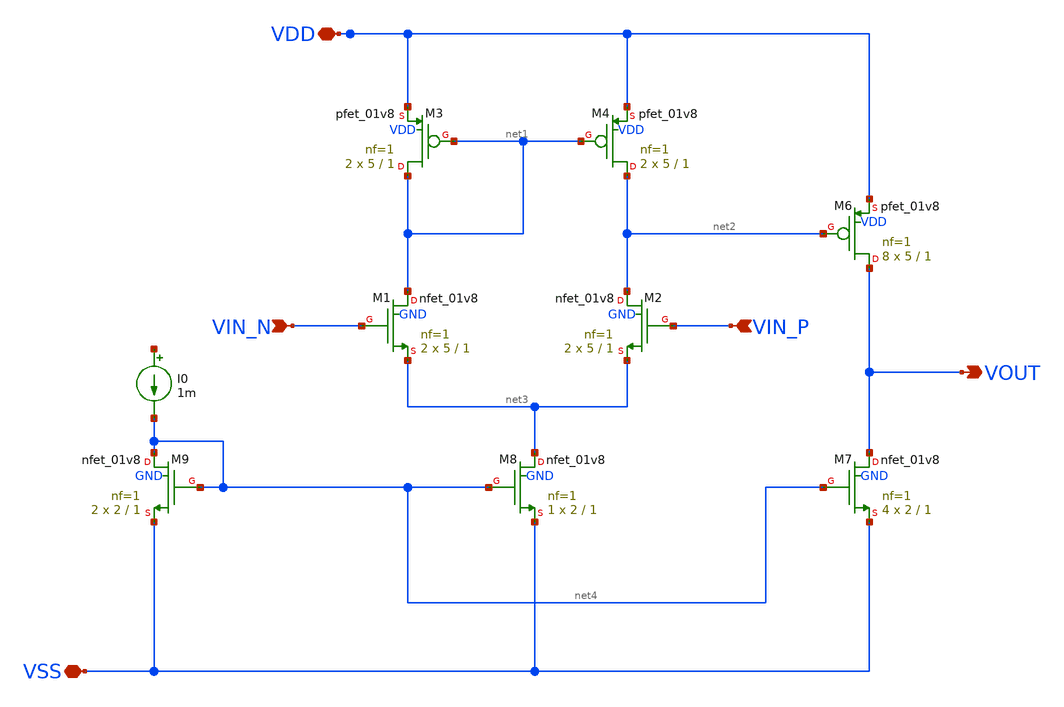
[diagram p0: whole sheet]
** sch_path: analog/schematics/opamp_two_stage.sch
**.subckt opamp_two_stage VDD VSS VOUT VIN_P VIN_N
*.iopin VDD
*.iopin VSS
*.opin VOUT
*.ipin VIN_P
*.ipin VIN_N
XM1 net1 VIN_N net3 GND sky130_fd_pr__nfet_01v8 L=1 W=5 nf=1 ad='int((nf+1)/2) * W/nf * 0.29' as='int((nf+2)/2) * W/nf * 0.29'
+ pd='2*int((nf+1)/2) * (W/nf + 0.29)' ps='2*int((nf+2)/2) * (W/nf + 0.29)' nrd='0.29 / W' nrs='0.29 / W'
+ sa=0 sb=0 sd=0 mult=2 m=2
XM2 net2 VIN_P net3 GND sky130_fd_pr__nfet_01v8 L=1 W=5 nf=1 ad='int((nf+1)/2) * W/nf * 0.29' as='int((nf+2)/2) * W/nf * 0.29'
+ pd='2*int((nf+1)/2) * (W/nf + 0.29)' ps='2*int((nf+2)/2) * (W/nf + 0.29)' nrd='0.29 / W' nrs='0.29 / W'
+ sa=0 sb=0 sd=0 mult=2 m=2
XM7 VOUT net4 VSS GND sky130_fd_pr__nfet_01v8 L=1 W=2 nf=1 ad='int((nf+1)/2) * W/nf * 0.29' as='int((nf+2)/2) * W/nf * 0.29'
+ pd='2*int((nf+1)/2) * (W/nf + 0.29)' ps='2*int((nf+2)/2) * (W/nf + 0.29)' nrd='0.29 / W' nrs='0.29 / W'
+ sa=0 sb=0 sd=0 mult=4 m=4
XM8 net3 net4 VSS GND sky130_fd_pr__nfet_01v8 L=1 W=2 nf=1 ad='int((nf+1)/2) * W/nf * 0.29' as='int((nf+2)/2) * W/nf * 0.29'
+ pd='2*int((nf+1)/2) * (W/nf + 0.29)' ps='2*int((nf+2)/2) * (W/nf + 0.29)' nrd='0.29 / W' nrs='0.29 / W'
+ sa=0 sb=0 sd=0 mult=1 m=1
XM3 net1 net1 VDD VDD sky130_fd_pr__pfet_01v8 L=1 W=5 nf=1 ad='int((nf+1)/2) * W/nf * 0.29' as='int((nf+2)/2) * W/nf * 0.29'
+ pd='2*int((nf+1)/2) * (W/nf + 0.29)' ps='2*int((nf+2)/2) * (W/nf + 0.29)' nrd='0.29 / W' nrs='0.29 / W'
+ sa=0 sb=0 sd=0 mult=2 m=2
XM6 VOUT net2 VDD VDD sky130_fd_pr__pfet_01v8 L=1 W=5 nf=1 ad='int((nf+1)/2) * W/nf * 0.29' as='int((nf+2)/2) * W/nf * 0.29'
+ pd='2*int((nf+1)/2) * (W/nf + 0.29)' ps='2*int((nf+2)/2) * (W/nf + 0.29)' nrd='0.29 / W' nrs='0.29 / W'
+ sa=0 sb=0 sd=0 mult=8 m=8
XM4 net2 net1 VDD VDD sky130_fd_pr__pfet_01v8 L=1 W=5 nf=1 ad='int((nf+1)/2) * W/nf * 0.29' as='int((nf+2)/2) * W/nf * 0.29'
+ pd='2*int((nf+1)/2) * (W/nf + 0.29)' ps='2*int((nf+2)/2) * (W/nf + 0.29)' nrd='0.29 / W' nrs='0.29 / W'
+ sa=0 sb=0 sd=0 mult=2 m=2
XM9 net4 net4 VSS GND sky130_fd_pr__nfet_01v8 L=1 W=2 nf=1 ad='int((nf+1)/2) * W/nf * 0.29' as='int((nf+2)/2) * W/nf * 0.29'
+ pd='2*int((nf+1)/2) * (W/nf + 0.29)' ps='2*int((nf+2)/2) * (W/nf + 0.29)' nrd='0.29 / W' nrs='0.29 / W'
+ sa=0 sb=0 sd=0 mult=2 m=2
I0 net5 net4 1m
**.ends
.end
